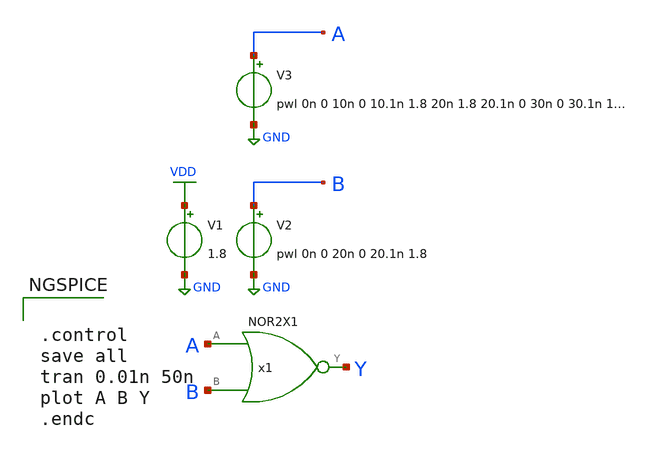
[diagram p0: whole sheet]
** sch_path: lib/xschem/test_NOR2X1.sch
**.subckt test_NOR2X1
V2 B GND pwl 0n 0 20n 0 20.1n 1.8
V1 VDD GND 1.8
V3 A GND pwl 0n 0 10n 0 10.1n 1.8 20n 1.8 20.1n 0 30n 0 30.1n 1.8 40n 1.8 40.1n 0
x1 Y A B VDD GND NOR2X1
**** begin user architecture code

.lib $::SKYWATER_MODELS/sky130.lib.spice tt


**** end user architecture code
**.ends

* expanding   symbol:  NOR2X1.sym # of pins=3
** sym_path: lib/xschem/NOR2X1.sym
** sch_path: lib/xschem/NOR2X1.sch
.subckt NOR2X1 Y A B VCCPIN VSSPIN
*.ipin A
*.opin Y
*.ipin B
XM1 Y A VSSPIN VSSPIN sky130_fd_pr__nfet_01v8 L=0.15 W=3 nf=1 ad='int((nf+1)/2) * W/nf * 0.29' as='int((nf+2)/2) * W/nf * 0.29'
+ pd='2*int((nf+1)/2) * (W/nf + 0.29)' ps='2*int((nf+2)/2) * (W/nf + 0.29)' nrd='0.29 / W' nrs='0.29 / W'
+ sa=0 sb=0 sd=0 mult=1 m=1
XM2 net1 A VCCPIN VCCPIN sky130_fd_pr__pfet_01v8 L=0.15 W=2 nf=1 ad='int((nf+1)/2) * W/nf * 0.29' as='int((nf+2)/2) * W/nf * 0.29'
+ pd='2*int((nf+1)/2) * (W/nf + 0.29)' ps='2*int((nf+2)/2) * (W/nf + 0.29)' nrd='0.29 / W' nrs='0.29 / W'
+ sa=0 sb=0 sd=0 mult=1 m=1
XM3 Y B VSSPIN VSSPIN sky130_fd_pr__nfet_01v8 L=0.15 W=3 nf=1 ad='int((nf+1)/2) * W/nf * 0.29' as='int((nf+2)/2) * W/nf * 0.29'
+ pd='2*int((nf+1)/2) * (W/nf + 0.29)' ps='2*int((nf+2)/2) * (W/nf + 0.29)' nrd='0.29 / W' nrs='0.29 / W'
+ sa=0 sb=0 sd=0 mult=1 m=1
XM4 net1 A VCCPIN VCCPIN sky130_fd_pr__pfet_01v8 L=0.15 W=2 nf=1 ad='int((nf+1)/2) * W/nf * 0.29' as='int((nf+2)/2) * W/nf * 0.29'
+ pd='2*int((nf+1)/2) * (W/nf + 0.29)' ps='2*int((nf+2)/2) * (W/nf + 0.29)' nrd='0.29 / W' nrs='0.29 / W'
+ sa=0 sb=0 sd=0 mult=1 m=1
XM5 Y B net1 VCCPIN sky130_fd_pr__pfet_01v8 L=0.15 W=2 nf=1 ad='int((nf+1)/2) * W/nf * 0.29' as='int((nf+2)/2) * W/nf * 0.29'
+ pd='2*int((nf+1)/2) * (W/nf + 0.29)' ps='2*int((nf+2)/2) * (W/nf + 0.29)' nrd='0.29 / W' nrs='0.29 / W'
+ sa=0 sb=0 sd=0 mult=1 m=1
XM6 Y B net1 VCCPIN sky130_fd_pr__pfet_01v8 L=0.15 W=2 nf=1 ad='int((nf+1)/2) * W/nf * 0.29' as='int((nf+2)/2) * W/nf * 0.29'
+ pd='2*int((nf+1)/2) * (W/nf + 0.29)' ps='2*int((nf+2)/2) * (W/nf + 0.29)' nrd='0.29 / W' nrs='0.29 / W'
+ sa=0 sb=0 sd=0 mult=1 m=1
.ends

.GLOBAL VDD
.GLOBAL GND
**** begin user architecture code


.control
save all
tran 0.01n 50n
plot A B Y
.endc


**** end user architecture code
.end
